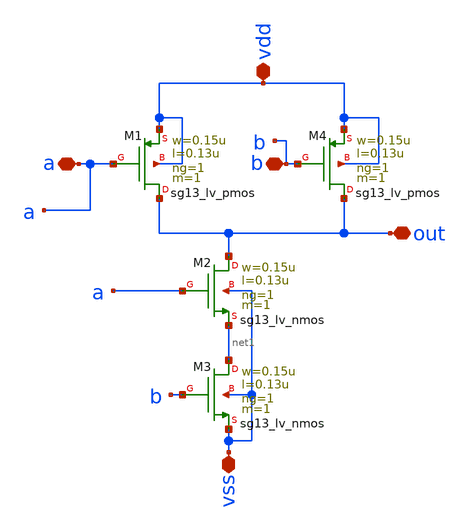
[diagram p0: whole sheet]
** sch_path: design/blocks/nandgate/schematic/nand.sch
**.subckt nand vdd a vss out b
*.iopin vdd
*.iopin a
*.iopin vss
*.iopin out
*.iopin b
XM1 out a vdd vdd sg13_lv_pmos w=0.15u l=0.13u ng=1 m=1 mm_ok=1
XM2 out a net1 vss sg13_lv_nmos w=0.15u l=0.13u ng=1 m=1 mm_ok=1
XM3 net1 b vss vss sg13_lv_nmos w=0.15u l=0.13u ng=1 m=1 mm_ok=1
XM4 out b vdd vdd sg13_lv_pmos w=0.15u l=0.13u ng=1 m=1 mm_ok=1
**.ends
.end
